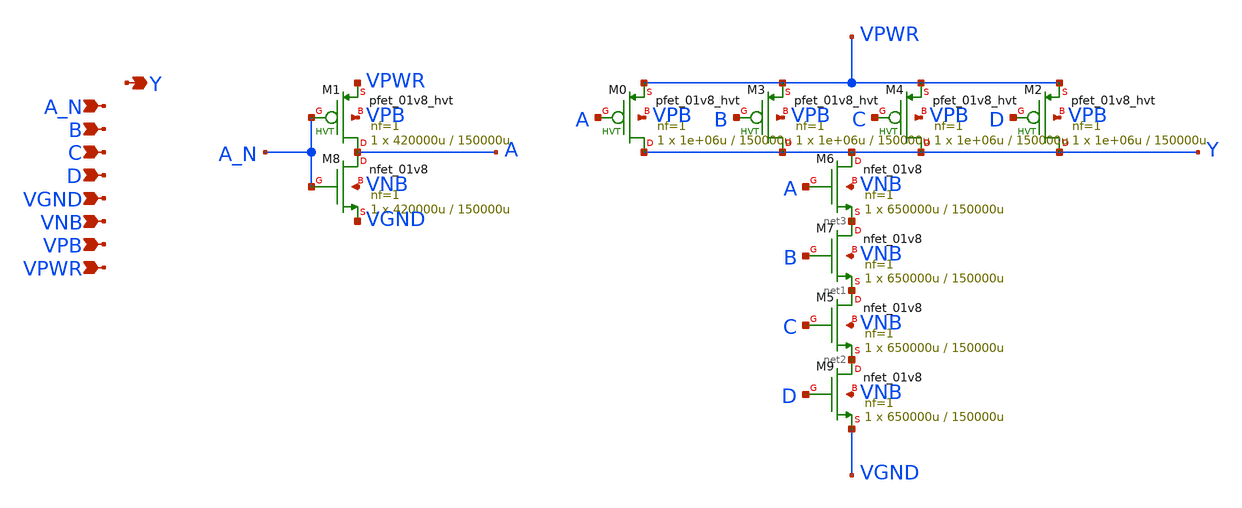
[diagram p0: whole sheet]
** sch_path: schematics/nand4b/sky130_fd_sc_hd__nand4b_1.sch
**.subckt sky130_fd_sc_hd__nand4b_1 A_N B C D VGND VNB VPB VPWR Y
*.ipin A_N
*.ipin B
*.ipin C
*.ipin D
*.ipin VGND
*.ipin VNB
*.ipin VPB
*.ipin VPWR
*.opin Y
XM0 Y A VPWR VPB sky130_fd_pr__pfet_01v8_hvt L=150000u W=1e+06u nf=1 ad='int((1 + 1)/2) * 1e+06u / 1 * 0.29'
+ as='int((1 + 2)/2) * 1e+06u / 1 * 0.29' pd='2*int((1 + 1)/2) * (1e+06u / 1 + 0.29)' ps='2*int((1 + 2)/2) * (1e+06u / 1 + 0.29)'
+ nrd='0.29 / 1e+06u ' nrs='0.29 / 1e+06u ' sa=0 sb=0 sd=0 mult=1 m=1
XM1 A A_N VPWR VPB sky130_fd_pr__pfet_01v8_hvt L=150000u W=420000u nf=1 ad='int((1 + 1)/2) * 420000u / 1 * 0.29'
+ as='int((1 + 2)/2) * 420000u / 1 * 0.29' pd='2*int((1 + 1)/2) * (420000u / 1 + 0.29)' ps='2*int((1 + 2)/2) * (420000u / 1 + 0.29)'
+ nrd='0.29 / 420000u ' nrs='0.29 / 420000u ' sa=0 sb=0 sd=0 mult=1 m=1
XM2 Y D VPWR VPB sky130_fd_pr__pfet_01v8_hvt L=150000u W=1e+06u nf=1 ad='int((1 + 1)/2) * 1e+06u / 1 * 0.29'
+ as='int((1 + 2)/2) * 1e+06u / 1 * 0.29' pd='2*int((1 + 1)/2) * (1e+06u / 1 + 0.29)' ps='2*int((1 + 2)/2) * (1e+06u / 1 + 0.29)'
+ nrd='0.29 / 1e+06u ' nrs='0.29 / 1e+06u ' sa=0 sb=0 sd=0 mult=1 m=1
XM3 Y B VPWR VPB sky130_fd_pr__pfet_01v8_hvt L=150000u W=1e+06u nf=1 ad='int((1 + 1)/2) * 1e+06u / 1 * 0.29'
+ as='int((1 + 2)/2) * 1e+06u / 1 * 0.29' pd='2*int((1 + 1)/2) * (1e+06u / 1 + 0.29)' ps='2*int((1 + 2)/2) * (1e+06u / 1 + 0.29)'
+ nrd='0.29 / 1e+06u ' nrs='0.29 / 1e+06u ' sa=0 sb=0 sd=0 mult=1 m=1
XM4 Y C VPWR VPB sky130_fd_pr__pfet_01v8_hvt L=150000u W=1e+06u nf=1 ad='int((1 + 1)/2) * 1e+06u / 1 * 0.29'
+ as='int((1 + 2)/2) * 1e+06u / 1 * 0.29' pd='2*int((1 + 1)/2) * (1e+06u / 1 + 0.29)' ps='2*int((1 + 2)/2) * (1e+06u / 1 + 0.29)'
+ nrd='0.29 / 1e+06u ' nrs='0.29 / 1e+06u ' sa=0 sb=0 sd=0 mult=1 m=1
XM5 net1 C net2 VNB sky130_fd_pr__nfet_01v8 L=150000u W=650000u nf=1 ad='int((1 + 1)/2) * 650000u / 1 * 0.29'
+ as='int((1 + 2)/2) * 650000u / 1 * 0.29' pd='2*int((1 + 1)/2) * (650000u / 1 + 0.29)' ps='2*int((1 + 2)/2) * (650000u / 1 + 0.29)'
+ nrd='0.29 / 650000u ' nrs='0.29 / 650000u ' sa=0 sb=0 sd=0 mult=1 m=1
XM6 Y A net3 VNB sky130_fd_pr__nfet_01v8 L=150000u W=650000u nf=1 ad='int((1 + 1)/2) * 650000u / 1 * 0.29'
+ as='int((1 + 2)/2) * 650000u / 1 * 0.29' pd='2*int((1 + 1)/2) * (650000u / 1 + 0.29)' ps='2*int((1 + 2)/2) * (650000u / 1 + 0.29)'
+ nrd='0.29 / 650000u ' nrs='0.29 / 650000u ' sa=0 sb=0 sd=0 mult=1 m=1
XM7 net3 B net1 VNB sky130_fd_pr__nfet_01v8 L=150000u W=650000u nf=1 ad='int((1 + 1)/2) * 650000u / 1 * 0.29'
+ as='int((1 + 2)/2) * 650000u / 1 * 0.29' pd='2*int((1 + 1)/2) * (650000u / 1 + 0.29)' ps='2*int((1 + 2)/2) * (650000u / 1 + 0.29)'
+ nrd='0.29 / 650000u ' nrs='0.29 / 650000u ' sa=0 sb=0 sd=0 mult=1 m=1
XM8 A A_N VGND VNB sky130_fd_pr__nfet_01v8 L=150000u W=420000u nf=1 ad='int((1 + 1)/2) * 420000u / 1 * 0.29'
+ as='int((1 + 2)/2) * 420000u / 1 * 0.29' pd='2*int((1 + 1)/2) * (420000u / 1 + 0.29)' ps='2*int((1 + 2)/2) * (420000u / 1 + 0.29)'
+ nrd='0.29 / 420000u ' nrs='0.29 / 420000u ' sa=0 sb=0 sd=0 mult=1 m=1
XM9 net2 D VGND VNB sky130_fd_pr__nfet_01v8 L=150000u W=650000u nf=1 ad='int((1 + 1)/2) * 650000u / 1 * 0.29'
+ as='int((1 + 2)/2) * 650000u / 1 * 0.29' pd='2*int((1 + 1)/2) * (650000u / 1 + 0.29)' ps='2*int((1 + 2)/2) * (650000u / 1 + 0.29)'
+ nrd='0.29 / 650000u ' nrs='0.29 / 650000u ' sa=0 sb=0 sd=0 mult=1 m=1
**.ends
.end
